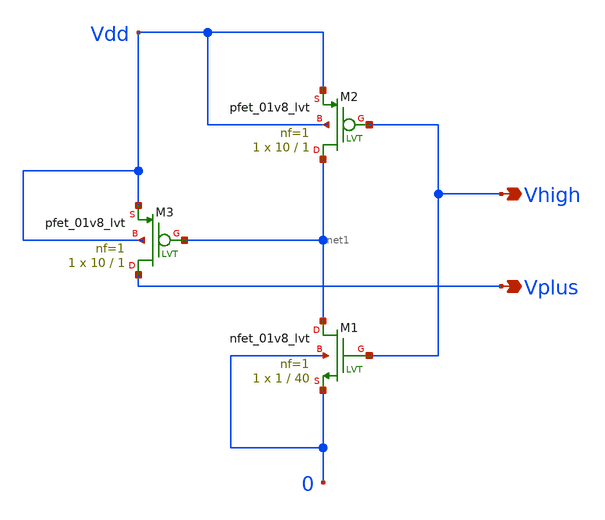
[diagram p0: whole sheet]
** sch_path: Bandgap/My Design/Schematics/Startup1.8v.sch
**.subckt Startup1.8v Vhigh Vplus
*.opin Vhigh
*.opin Vplus
XM1 net1 Vhigh 0 0 sky130_fd_pr__nfet_01v8_lvt L=40 W=1 nf=1 ad='int((nf+1)/2) * W/nf * 0.29' as='int((nf+2)/2) * W/nf * 0.29'
+ pd='2*int((nf+1)/2) * (W/nf + 0.29)' ps='2*int((nf+2)/2) * (W/nf + 0.29)' nrd='0.29 / W' nrs='0.29 / W'
+ sa=0 sb=0 sd=0 mult=1 m=1
XM2 net1 Vhigh Vdd Vdd sky130_fd_pr__pfet_01v8_lvt L=1 W=10 nf=1 ad='int((nf+1)/2) * W/nf * 0.29' as='int((nf+2)/2) * W/nf * 0.29'
+ pd='2*int((nf+1)/2) * (W/nf + 0.29)' ps='2*int((nf+2)/2) * (W/nf + 0.29)' nrd='0.29 / W' nrs='0.29 / W'
+ sa=0 sb=0 sd=0 mult=1 m=1
XM3 Vplus net1 Vdd Vdd sky130_fd_pr__pfet_01v8_lvt L=1 W=10 nf=1 ad='int((nf+1)/2) * W/nf * 0.29' as='int((nf+2)/2) * W/nf * 0.29'
+ pd='2*int((nf+1)/2) * (W/nf + 0.29)' ps='2*int((nf+2)/2) * (W/nf + 0.29)' nrd='0.29 / W' nrs='0.29 / W'
+ sa=0 sb=0 sd=0 mult=1 m=1
**.ends
.end
